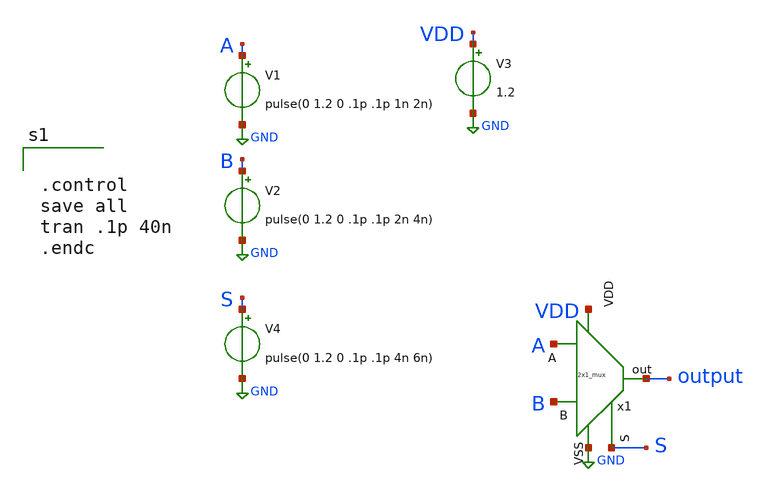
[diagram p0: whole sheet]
** sch_path: 2x1_mux/2x1_mux_tb.sch
**.subckt 2x1_mux_tb
x1 B VDD A GND S output 2x1_mux
V1 A GND pulse(0 1.2 0 .1p .1p 1n 2n)
V2 B GND pulse(0 1.2 0 .1p .1p 2n 4n)
V3 VDD GND 1.2
V4 S GND pulse(0 1.2 0 .1p .1p 4n 6n)
**** begin user architecture code

** opencircuitdesign pdks install
.lib $::SKYWATER_MODELS/sky130.lib.spice tt




.control
save all
tran .1p 40n
.endc

**** end user architecture code
**.ends

* expanding   symbol:  2x1_mux.sym # of pins=6
** sym_path: 2x1_mux/2x1_mux.sym
** sch_path: 2x1_mux/2x1_mux.sch
.subckt 2x1_mux B VDD A VSS S out
*.ipin VDD
*.ipin A
*.ipin B
*.opin out
*.ipin S
*.ipin VSS
XM1 net1 A net4 net4 sky130_fd_pr__nfet_01v8 L=0.15 W=1 nf=1 ad='int((nf+1)/2) * W/nf * 0.29' as='int((nf+2)/2) * W/nf * 0.29'
+ pd='2*int((nf+1)/2) * (W/nf + 0.29)' ps='2*int((nf+2)/2) * (W/nf + 0.29)' nrd='0.29 / W' nrs='0.29 / W'
+ sa=0 sb=0 sd=0 mult=1 m=1
XM2 net3 A VDD VDD sky130_fd_pr__pfet_01v8 L=0.15 W=1 nf=1 ad='int((nf+1)/2) * W/nf * 0.29' as='int((nf+2)/2) * W/nf * 0.29'
+ pd='2*int((nf+1)/2) * (W/nf + 0.29)' ps='2*int((nf+2)/2) * (W/nf + 0.29)' nrd='0.29 / W' nrs='0.29 / W'
+ sa=0 sb=0 sd=0 mult=1 m=1
XM3 net2 notS VDD VDD sky130_fd_pr__pfet_01v8 L=0.15 W=1 nf=1 ad='int((nf+1)/2) * W/nf * 0.29' as='int((nf+2)/2) * W/nf * 0.29'
+ pd='2*int((nf+1)/2) * (W/nf + 0.29)' ps='2*int((nf+2)/2) * (W/nf + 0.29)' nrd='0.29 / W' nrs='0.29 / W'
+ sa=0 sb=0 sd=0 mult=1 m=1
XM4 net1 B net3 net3 sky130_fd_pr__pfet_01v8 L=0.15 W=1 nf=1 ad='int((nf+1)/2) * W/nf * 0.29' as='int((nf+2)/2) * W/nf * 0.29'
+ pd='2*int((nf+1)/2) * (W/nf + 0.29)' ps='2*int((nf+2)/2) * (W/nf + 0.29)' nrd='0.29 / W' nrs='0.29 / W'
+ sa=0 sb=0 sd=0 mult=1 m=1
XM5 net1 S net2 net2 sky130_fd_pr__pfet_01v8 L=0.15 W=1 nf=1 ad='int((nf+1)/2) * W/nf * 0.29' as='int((nf+2)/2) * W/nf * 0.29'
+ pd='2*int((nf+1)/2) * (W/nf + 0.29)' ps='2*int((nf+2)/2) * (W/nf + 0.29)' nrd='0.29 / W' nrs='0.29 / W'
+ sa=0 sb=0 sd=0 mult=1 m=1
XM6 net1 B net5 net5 sky130_fd_pr__nfet_01v8 L=0.15 W=1 nf=1 ad='int((nf+1)/2) * W/nf * 0.29' as='int((nf+2)/2) * W/nf * 0.29'
+ pd='2*int((nf+1)/2) * (W/nf + 0.29)' ps='2*int((nf+2)/2) * (W/nf + 0.29)' nrd='0.29 / W' nrs='0.29 / W'
+ sa=0 sb=0 sd=0 mult=1 m=1
XM7 net4 notS VSS VSS sky130_fd_pr__nfet_01v8 L=0.15 W=1 nf=1 ad='int((nf+1)/2) * W/nf * 0.29' as='int((nf+2)/2) * W/nf * 0.29'
+ pd='2*int((nf+1)/2) * (W/nf + 0.29)' ps='2*int((nf+2)/2) * (W/nf + 0.29)' nrd='0.29 / W' nrs='0.29 / W'
+ sa=0 sb=0 sd=0 mult=1 m=1
XM8 net5 S VSS VSS sky130_fd_pr__nfet_01v8 L=0.15 W=1 nf=1 ad='int((nf+1)/2) * W/nf * 0.29' as='int((nf+2)/2) * W/nf * 0.29'
+ pd='2*int((nf+1)/2) * (W/nf + 0.29)' ps='2*int((nf+2)/2) * (W/nf + 0.29)' nrd='0.29 / W' nrs='0.29 / W'
+ sa=0 sb=0 sd=0 mult=1 m=1
XM9 notS S VSS VSS sky130_fd_pr__nfet_01v8 L=0.15 W=1 nf=1 ad='int((nf+1)/2) * W/nf * 0.29' as='int((nf+2)/2) * W/nf * 0.29'
+ pd='2*int((nf+1)/2) * (W/nf + 0.29)' ps='2*int((nf+2)/2) * (W/nf + 0.29)' nrd='0.29 / W' nrs='0.29 / W'
+ sa=0 sb=0 sd=0 mult=1 m=1
XM10 notS S VDD VDD sky130_fd_pr__pfet_01v8 L=0.15 W=1 nf=1 ad='int((nf+1)/2) * W/nf * 0.29' as='int((nf+2)/2) * W/nf * 0.29'
+ pd='2*int((nf+1)/2) * (W/nf + 0.29)' ps='2*int((nf+2)/2) * (W/nf + 0.29)' nrd='0.29 / W' nrs='0.29 / W'
+ sa=0 sb=0 sd=0 mult=1 m=1
XM11 out net1 VSS VSS sky130_fd_pr__nfet_01v8 L=0.15 W=1 nf=1 ad='int((nf+1)/2) * W/nf * 0.29' as='int((nf+2)/2) * W/nf * 0.29'
+ pd='2*int((nf+1)/2) * (W/nf + 0.29)' ps='2*int((nf+2)/2) * (W/nf + 0.29)' nrd='0.29 / W' nrs='0.29 / W'
+ sa=0 sb=0 sd=0 mult=1 m=1
XM12 out net1 VDD VDD sky130_fd_pr__pfet_01v8 L=0.15 W=1 nf=1 ad='int((nf+1)/2) * W/nf * 0.29' as='int((nf+2)/2) * W/nf * 0.29'
+ pd='2*int((nf+1)/2) * (W/nf + 0.29)' ps='2*int((nf+2)/2) * (W/nf + 0.29)' nrd='0.29 / W' nrs='0.29 / W'
+ sa=0 sb=0 sd=0 mult=1 m=1
.ends

.GLOBAL GND
.end
